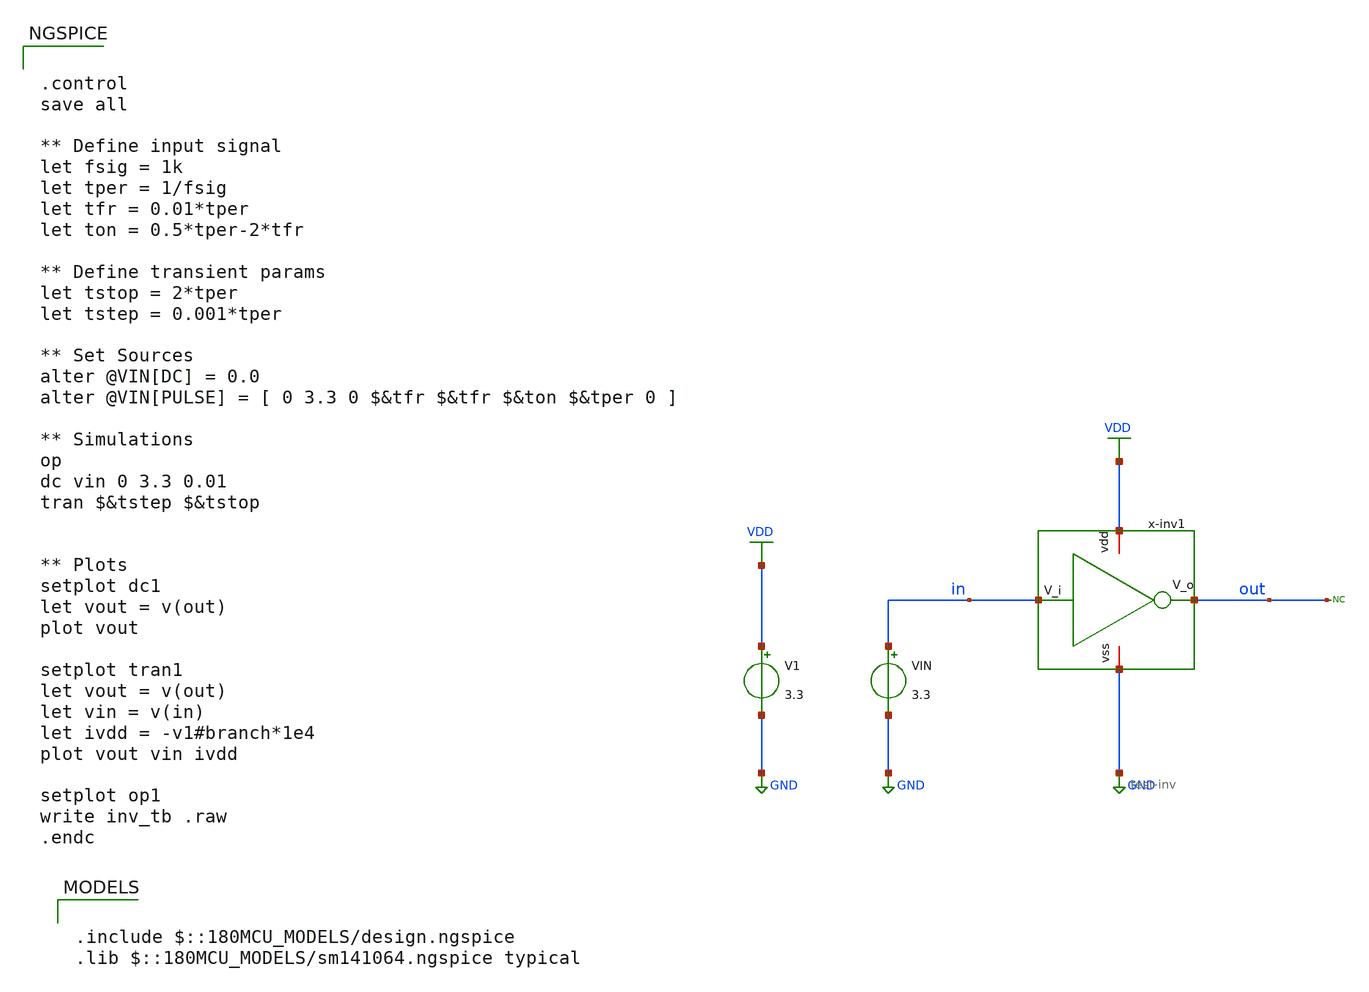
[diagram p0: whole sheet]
** sch_path: designs/test/test-inv_tb.sch
**.subckt test-inv_tb
V1 VDD GND 3.3
VIN in GND 3.3
* noconn out
x-inv1 VDD in out GND test-inv
**** begin user architecture code

.include $::180MCU_MODELS/design.ngspice
.lib $::180MCU_MODELS/sm141064.ngspice typical



.control
save all

** Define input signal
let fsig = 1k
let tper = 1/fsig
let tfr = 0.01*tper
let ton = 0.5*tper-2*tfr

** Define transient params
let tstop = 2*tper
let tstep = 0.001*tper

** Set Sources
alter @VIN[DC] = 0.0
alter @VIN[PULSE] = [ 0 3.3 0 $&tfr $&tfr $&ton $&tper 0 ]

** Simulations
op
dc vin 0 3.3 0.01
tran $&tstep $&tstop


** Plots
setplot dc1
let vout = v(out)
plot vout

setplot tran1
let vout = v(out)
let vin = v(in)
let ivdd = -v1#branch*1e4
plot vout vin ivdd

setplot op1
write inv_tb .raw
.endc


**** end user architecture code
**.ends

* expanding   symbol:  test/test-inv.sym # of pins=4
** sym_path: designs/test/test-inv.sym
** sch_path: designs/test/test-inv.sch
.subckt test-inv vdd V_i V_o vss
*.iopin vdd
*.iopin vss
*.ipin V_i
*.opin V_o
XM1 V_o V_i vss vss nfet_03v3 L=0.28u W=0.22u nf=1 ad='int((nf+1)/2) * W/nf * 0.18u' as='int((nf+2)/2) * W/nf * 0.18u'
+ pd='2*int((nf+1)/2) * (W/nf + 0.18u)' ps='2*int((nf+2)/2) * (W/nf + 0.18u)' nrd='0.18u / W' nrs='0.18u / W'
+ sa=0 sb=0 sd=0 m=1
XM2 V_o V_i vdd vdd pfet_03v3 L=0.28u W=0.22u nf=1 ad='int((nf+1)/2) * W/nf * 0.18u' as='int((nf+2)/2) * W/nf * 0.18u'
+ pd='2*int((nf+1)/2) * (W/nf + 0.18u)' ps='2*int((nf+2)/2) * (W/nf + 0.18u)' nrd='0.18u / W' nrs='0.18u / W'
+ sa=0 sb=0 sd=0 m=1
.ends

.GLOBAL VDD
.GLOBAL GND
.end
